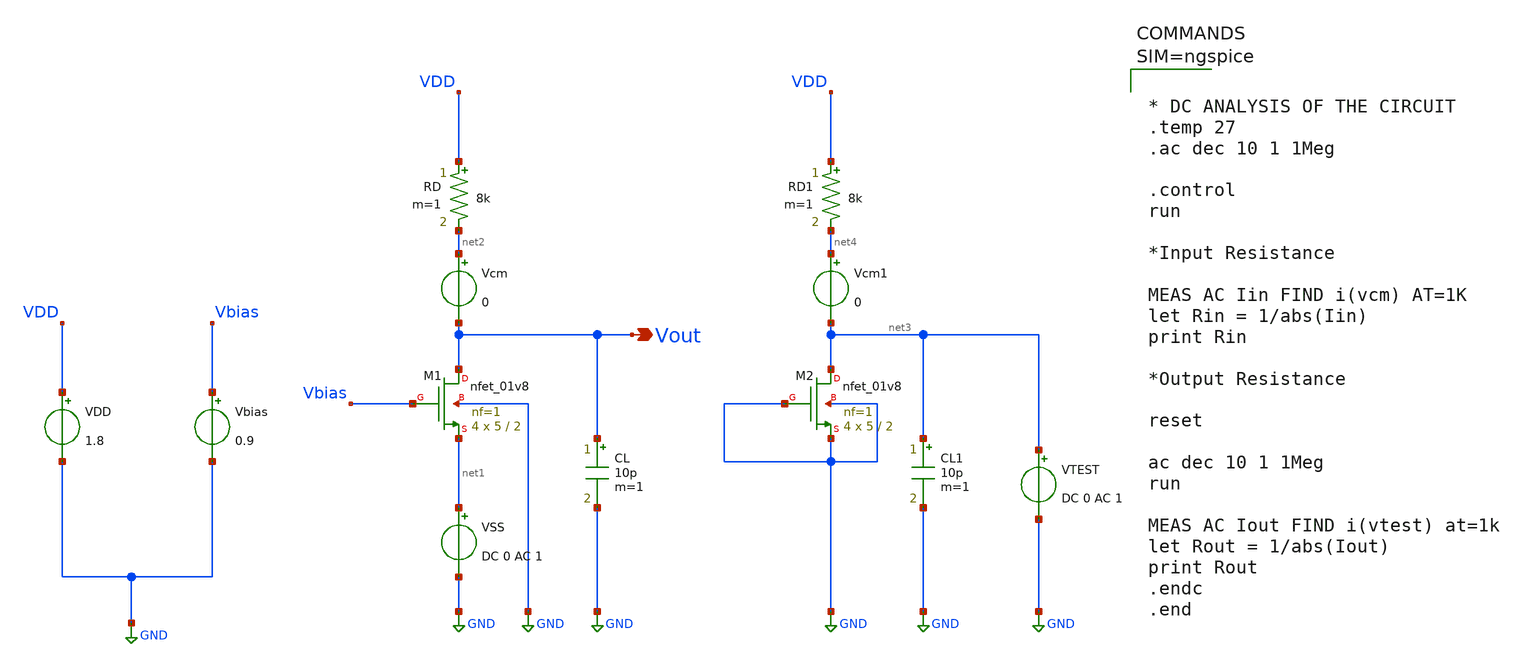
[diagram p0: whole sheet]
** sch_path: Common_Gate_MOS_Amps/Common_Gate_Amp_Rin_Rout_Finding.sch
**.subckt Common_Gate_Amp_Rin_Rout_Finding Vout
*.opin Vout
XM1 Vout Vbias net1 GND sky130_fd_pr__nfet_01v8 L=2 W=5 nf=1 ad='int((1 + 1)/2) * 5 / 1 * 0.29' as='int((1 + 2)/2) * 5 / 1 * 0.29'
+ pd='2*int((1 + 1)/2) * (5 / 1 + 0.29)' ps='2*int((1 + 2)/2) * (5 / 1 + 0.29)' nrd='0.29 / 5 ' nrs='0.29 / 5 '
+ sa=0 sb=0 sd=0 mult=4 m=4
RD VDD net2 8k m=1
CL Vout GND 10p m=1
VDD VDD GND 1.8
Vbias Vbias GND 0.9
VSS net1 GND DC 0 AC 1
Vcm net2 Vout 0
XM2 net3 GND GND GND sky130_fd_pr__nfet_01v8 L=2 W=5 nf=1 ad='int((1 + 1)/2) * 5 / 1 * 0.29' as='int((1 + 2)/2) * 5 / 1 * 0.29'
+ pd='2*int((1 + 1)/2) * (5 / 1 + 0.29)' ps='2*int((1 + 2)/2) * (5 / 1 + 0.29)' nrd='0.29 / 5 ' nrs='0.29 / 5 '
+ sa=0 sb=0 sd=0 mult=4 m=4
RD1 VDD net4 8k m=1
CL1 net3 GND 10p m=1
Vcm1 net4 net3 0
VTEST net3 GND DC 0 AC 1
**** begin user architecture code

** opencircuitdesign pdks install
.lib $::SKYWATER_MODELS/sky130.lib.spice tt




* DC ANALYSIS OF THE CIRCUIT
.temp 27
.ac dec 10 1 1Meg

.control
run

*Input Resistance

MEAS AC Iin FIND i(vcm) AT=1K
let Rin = 1/abs(Iin)
print Rin

*Output Resistance

reset

ac dec 10 1 1Meg
run

MEAS AC Iout FIND i(vtest) at=1k
let Rout = 1/abs(Iout)
print Rout
.endc
.end




**** end user architecture code
**.ends
.GLOBAL GND
.end
